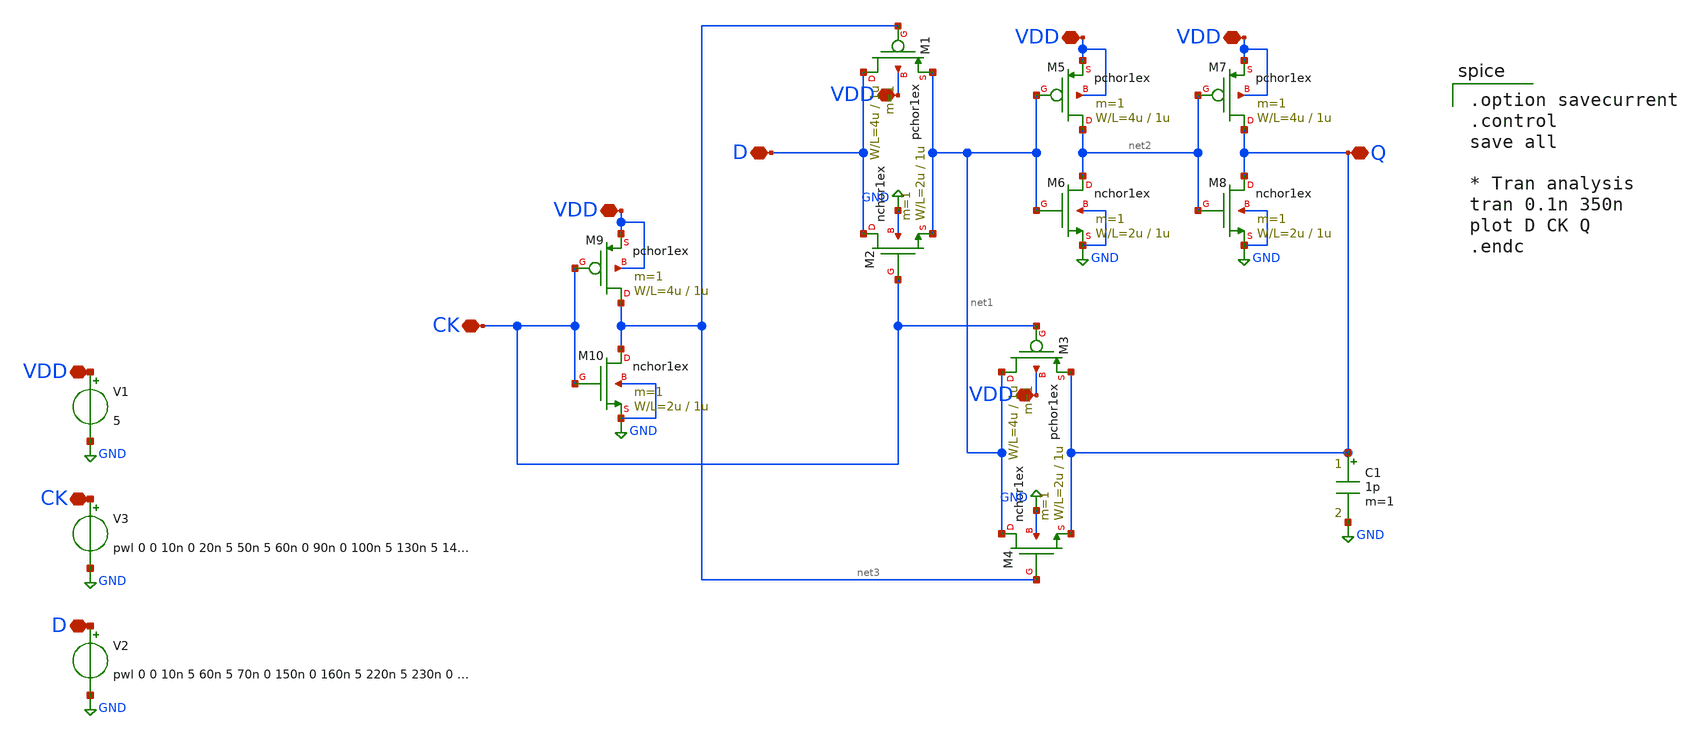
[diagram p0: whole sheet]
** sch_path: member_project/dokunira/Dlatch_layout/Dlatch_sim.sch
**.subckt Dlatch_sim CK D VDD VDD VDD Q VDD D CK VDD VDD
*.iopin CK
*.iopin D
*.iopin VDD
*.iopin VDD
*.iopin VDD
*.iopin Q
*.iopin VDD
*.iopin D
*.iopin CK
*.iopin VDD
*.iopin VDD
M1 D net3 net1 VDD pchor1ex L=1u W=4u m=1
M2 D CK net1 GND nchor1ex L=1u W=2u m=1
M3 net1 CK Q VDD pchor1ex L=1u W=4u m=1
M4 net1 net3 Q GND nchor1ex L=1u W=2u m=1
M5 net2 net1 VDD VDD pchor1ex L=1u W=4u m=1
M6 net2 net1 GND GND nchor1ex L=1u W=2u m=1
M7 Q net2 VDD VDD pchor1ex L=1u W=4u m=1
M8 Q net2 GND GND nchor1ex L=1u W=2u m=1
M9 net3 CK VDD VDD pchor1ex L=1u W=4u m=1
M10 net3 CK GND GND nchor1ex L=1u W=2u m=1
V1 VDD GND 5
V2 D GND pwl 0 0 10n 5 60n 5 70n 0 150n 0 160n 5 220n 5 230n 0 240n 0 250n 5 270n 5 280n 0 300n 0
+ 310n 5 330n 5 340n 0
V3 CK GND pwl 0 0 10n 0 20n 5 50n 5 60n 0 90n 0 100n 5 130n 5 140n 0 170n 0 180n 5 210n 5 220n 0
+ 280n 0 290n 5 350n 5
C1 Q GND 1p m=1
**** begin user architecture code
 .include $::LIB/mos.lib
.include $::LIB/passive.lib
.include $::LIB/diode.lib

.option savecurrent
.control
save all

* Tran analysis
tran 0.1n 350n
plot D CK Q
.endc


**** end user architecture code
**.ends
.GLOBAL GND
.end
